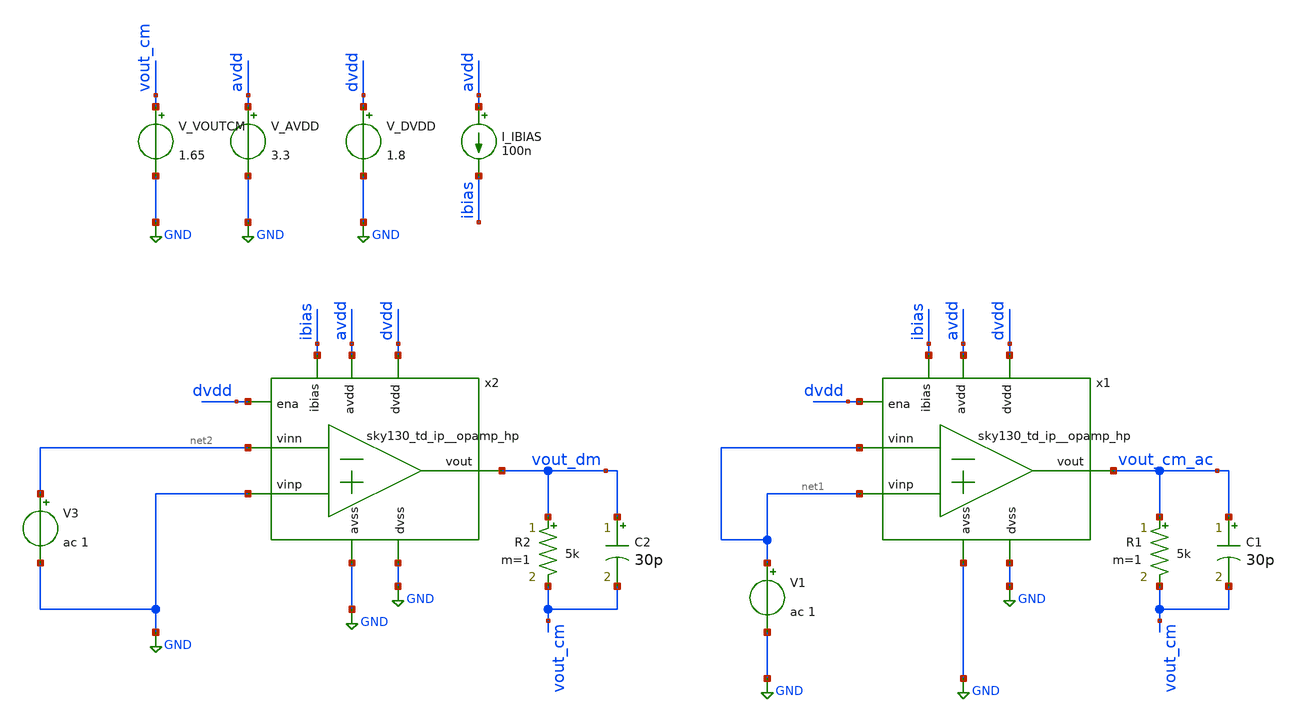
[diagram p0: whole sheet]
** sch_path: xschem/cmrr.sch
**.subckt cmrr
x1 avdd vout_cm_ac ibias net1 net1 GND dvdd GND dvdd sky130_td_ip__opamp_hp
V_AVDD avdd GND 3.3
.save i(v_avdd)
V_DVDD dvdd GND 1.8
.save i(v_dvdd)
I_IBIAS avdd ibias 100n
R1 vout_cm_ac vout_cm 5k m=1
C1 vout_cm_ac vout_cm 30p m=1
V_VOUTCM vout_cm GND 1.65
.save i(v_voutcm)
V1 net1 GND ac 1
x2 avdd vout_dm ibias net2 GND GND dvdd GND dvdd sky130_td_ip__opamp_hp
R2 vout_dm vout_cm 5k m=1
C2 vout_dm vout_cm 30p m=1
V3 net2 GND ac 1
**** begin user architecture code


.save all

.control
save all

* Run AC sweep from 1Hz to 1GHz
AC DEC 100 1 1000000000
run

* Get DC gain in DBs.
let adm_db = db(vout_dm)
let acm_db = db(vout_cm_ac)
let cmrr_db = adm_db - acm_db

meas AC cmrr_dc FIND cmrr_db AT=1
meas AC cmrr_100k FIND cmrr_db AT=100K

echo
echo ===================================
echo CMRR characterization results:
echo - CMRR @ 1 Hz: $&cmrr_dc
echo - CMRR @ 100 kHz: $&cmrr_100k
echo ===================================


plot cmrr_db

.endc




.lib /usr/local/share/pdk/sky130A/libs.tech/combined/sky130.lib.spice tt


**** end user architecture code
**.ends
.GLOBAL GND
.end
